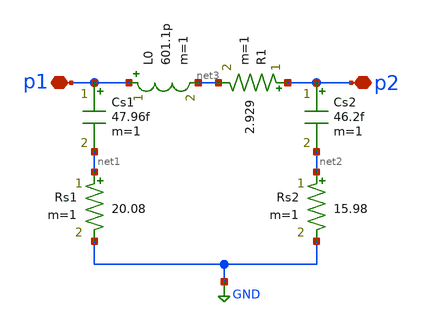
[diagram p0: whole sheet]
** sch_path: impedance-transformer/xschem/l1.sch
**.subckt l1 p2 p1
*.iopin p2
*.iopin p1
L0 p1 net3 601.1p m=1
Cs1 p1 net1 47.96f m=1
Cs2 p2 net2 46.2f m=1
Rs1 net1 GND 20.08 m=1
Rs2 net2 GND 15.98 m=1
R1 p2 net3 2.929 m=1
**.ends
.GLOBAL GND
.end
